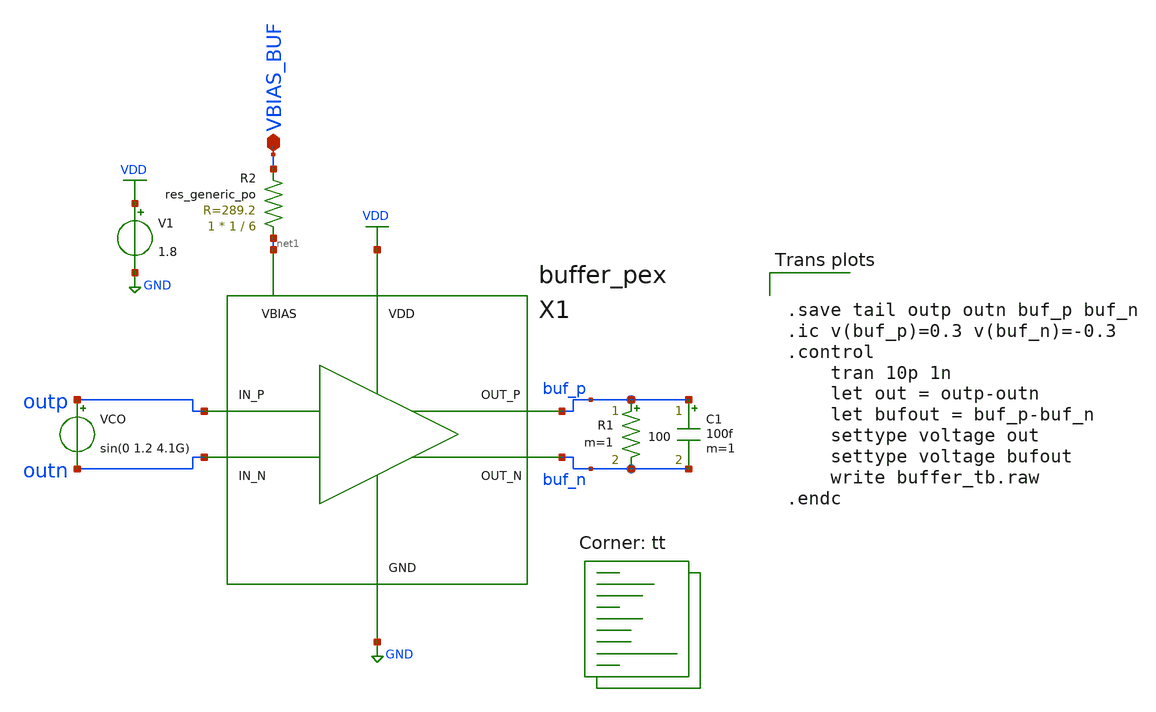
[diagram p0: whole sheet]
** sch_path: xschem/vco/testbenches/buffer/pex/buffer_tb_pex.sch
* YI/C9Shc8z/CWPKLJb8BQD+O4ziO4wpAwbu7u7s7HEAy2IIt2IIlQD6O4ziO4ypAAICtDl/GPL8AgNZy7Go7vwAAAAAAAAAAAAAAAAAAAAAAAPeMn2NHvywNosQhFFq
**.subckt buffer_tb_pex VBIAS_BUF
*.iopin VBIAS_BUF
R1 buf_p buf_n 100 m=1
C1 buf_p buf_n 100f m=1
V1 VDD GND 1.8
VCO outp outn sin(0 1.2 4.1G)
X1 net1 VDD GND buf_n buf_p outp outn buffer_pex
XR2 net1 VBIAS_BUF sky130_fd_pr__res_generic_po W=1 L=6 m=1
**** begin user architecture code


.save tail outp outn buf_p buf_n
.ic v(buf_p)=0.3 v(buf_n)=-0.3
.control
    tran 10p 1n
    let out = outp-outn
    let bufout = buf_p-buf_n
    settype voltage out
    settype voltage bufout
    write buffer_tb.raw
.endc


.lib $::SKYWATER_MODELS/sky130.lib.spice tt
**** end user architecture code
**.ends
.GLOBAL VDD
.GLOBAL GND
.end
